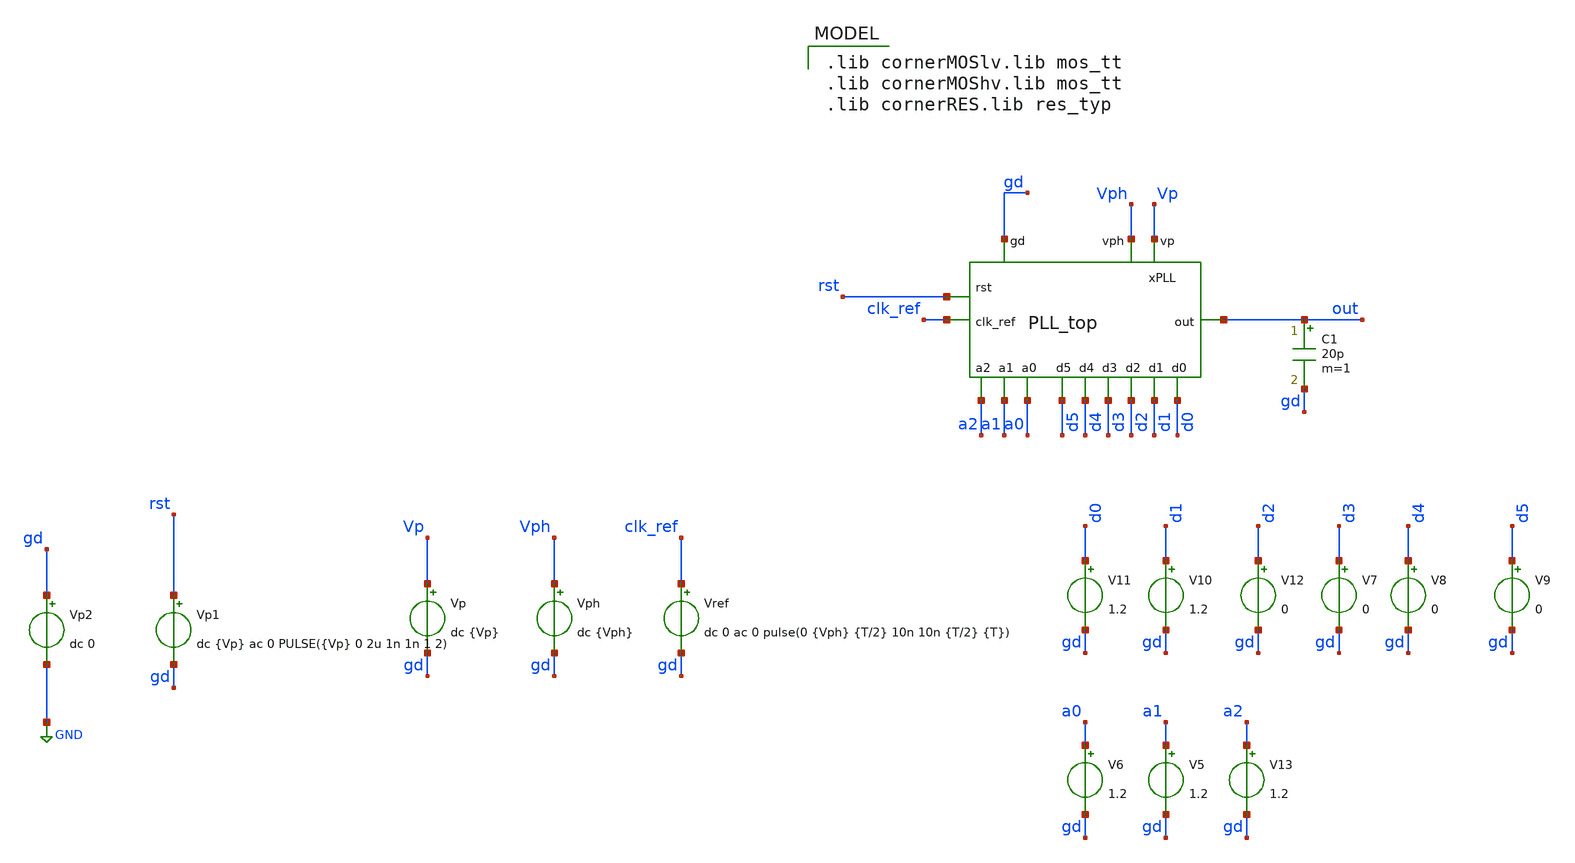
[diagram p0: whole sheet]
** sch_path: schematics/top/PLL_top_tb.sch
**.subckt PLL_top_tb
Vref clk_ref gd dc 0 ac 0 pulse(0 {Vph} {T/2} 10n 10n {T/2} {T})
Vp Vp gd dc {Vp}
Vph Vph gd dc {Vph}
C1 out gd 20p m=1
V8 d4 gd 0
V9 d5 gd 0
V11 d0 gd 1.2
V10 d1 gd 1.2
V12 d2 gd 0
V7 d3 gd 0
V5 a1 gd 1.2
V6 a0 gd 1.2
V13 a2 gd 1.2
xPLL Vp Vph gd clk_ref out d5 d3 a1 d2 d1 d0 d4 a2 a0 rst PLL_top
Vp1 rst gd dc {Vp} ac 0 PULSE({Vp} 0 2u 1n 1n 1 2)
Vp2 gd GND dc 0
**** begin user architecture code
 .lib cornerMOSlv.lib mos_tt
.lib cornerMOShv.lib mos_tt
.lib cornerRES.lib res_typ




.temp=25
.param T = 31.25u
.option klu method=gear reltol=1e-3 gmin=1e-12 abstol=1e-12 rshunt=1e12
.options cshunt=2.5f
.param Vp=1.2
.param Vph=3.3
.control

* Operating Point Analysis



write PLL_top_tb.raw
set appendwrite
save v(gd) v(vp) v(rst) v(out) v(xPLL.cvco) v(xPLL.cref) v(xPLL.UP) v(xPLL.DOWN) v(xPLL.vout)
+ v(xPLL.vco_out_prebuff) v(xPLL.vout_aftRC) v(xPLL.vco_out_buffered) v(xPLL.out_PLL_divided) v(xPLL.pre_LS) v(xPLL.aft_LS)
tran 0.1n 3m
meas tran t1 WHEN v(out)=1.65 RISE=1 FROM=0.7m
meas tran t2 WHEN v(out)=1.65 RISE=2 FROM=0.7m
meas tran period PARAM='t2-t1'
meas tran freq PARAM='1/period'

write PLL_top_tb.raw
.endc


**** end user architecture code
**.ends
.GLOBAL GND
.end
